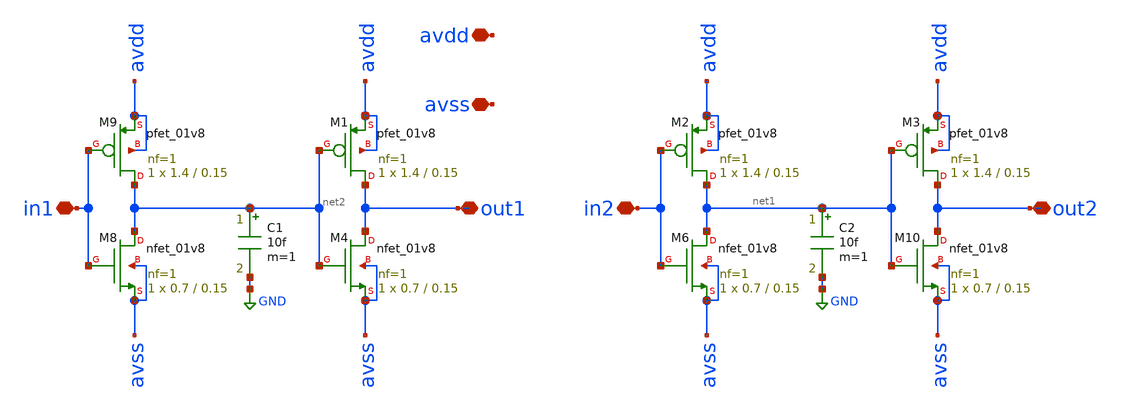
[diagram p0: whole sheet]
** sch_path: xschem/inv_buffer.sch
**.subckt inv_buffer in1 in2 out1 out2 avdd avss
*.iopin in1
*.iopin in2
*.iopin out1
*.iopin out2
*.iopin avdd
*.iopin avss
XM6 net1 in2 avss avss sky130_fd_pr__nfet_01v8 L=0.15 W=0.7 nf=1 ad='int((nf+1)/2) * W/nf * 0.29' as='int((nf+2)/2) * W/nf * 0.29'
+ pd='2*int((nf+1)/2) * (W/nf + 0.29)' ps='2*int((nf+2)/2) * (W/nf + 0.29)' nrd='0.29 / W' nrs='0.29 / W'
+ sa=0 sb=0 sd=0 mult=1 m=1
XM8 net2 in1 avss avss sky130_fd_pr__nfet_01v8 L=0.15 W=0.7 nf=1 ad='int((nf+1)/2) * W/nf * 0.29' as='int((nf+2)/2) * W/nf * 0.29'
+ pd='2*int((nf+1)/2) * (W/nf + 0.29)' ps='2*int((nf+2)/2) * (W/nf + 0.29)' nrd='0.29 / W' nrs='0.29 / W'
+ sa=0 sb=0 sd=0 mult=1 m=1
XM9 net2 in1 avdd avdd sky130_fd_pr__pfet_01v8 L=0.15 W=1.4 nf=1 ad='int((nf+1)/2) * W/nf * 0.29' as='int((nf+2)/2) * W/nf * 0.29'
+ pd='2*int((nf+1)/2) * (W/nf + 0.29)' ps='2*int((nf+2)/2) * (W/nf + 0.29)' nrd='0.29 / W' nrs='0.29 / W'
+ sa=0 sb=0 sd=0 mult=1 m=1
XM4 out1 net2 avss avss sky130_fd_pr__nfet_01v8 L=0.15 W=0.7 nf=1 ad='int((nf+1)/2) * W/nf * 0.29' as='int((nf+2)/2) * W/nf * 0.29'
+ pd='2*int((nf+1)/2) * (W/nf + 0.29)' ps='2*int((nf+2)/2) * (W/nf + 0.29)' nrd='0.29 / W' nrs='0.29 / W'
+ sa=0 sb=0 sd=0 mult=1 m=1
XM10 out2 net1 avss avss sky130_fd_pr__nfet_01v8 L=0.15 W=0.7 nf=1 ad='int((nf+1)/2) * W/nf * 0.29' as='int((nf+2)/2) * W/nf * 0.29'
+ pd='2*int((nf+1)/2) * (W/nf + 0.29)' ps='2*int((nf+2)/2) * (W/nf + 0.29)' nrd='0.29 / W' nrs='0.29 / W'
+ sa=0 sb=0 sd=0 mult=1 m=1
C1 net2 GND 10f m=1
C2 net1 GND 10f m=1
XM1 out1 net2 avdd avdd sky130_fd_pr__pfet_01v8 L=0.15 W=1.4 nf=1 ad='int((nf+1)/2) * W/nf * 0.29' as='int((nf+2)/2) * W/nf * 0.29'
+ pd='2*int((nf+1)/2) * (W/nf + 0.29)' ps='2*int((nf+2)/2) * (W/nf + 0.29)' nrd='0.29 / W' nrs='0.29 / W'
+ sa=0 sb=0 sd=0 mult=1 m=1
XM2 net1 in2 avdd avdd sky130_fd_pr__pfet_01v8 L=0.15 W=1.4 nf=1 ad='int((nf+1)/2) * W/nf * 0.29' as='int((nf+2)/2) * W/nf * 0.29'
+ pd='2*int((nf+1)/2) * (W/nf + 0.29)' ps='2*int((nf+2)/2) * (W/nf + 0.29)' nrd='0.29 / W' nrs='0.29 / W'
+ sa=0 sb=0 sd=0 mult=1 m=1
XM3 out2 net1 avdd avdd sky130_fd_pr__pfet_01v8 L=0.15 W=1.4 nf=1 ad='int((nf+1)/2) * W/nf * 0.29' as='int((nf+2)/2) * W/nf * 0.29'
+ pd='2*int((nf+1)/2) * (W/nf + 0.29)' ps='2*int((nf+2)/2) * (W/nf + 0.29)' nrd='0.29 / W' nrs='0.29 / W'
+ sa=0 sb=0 sd=0 mult=1 m=1
**.ends
.GLOBAL GND
.end
